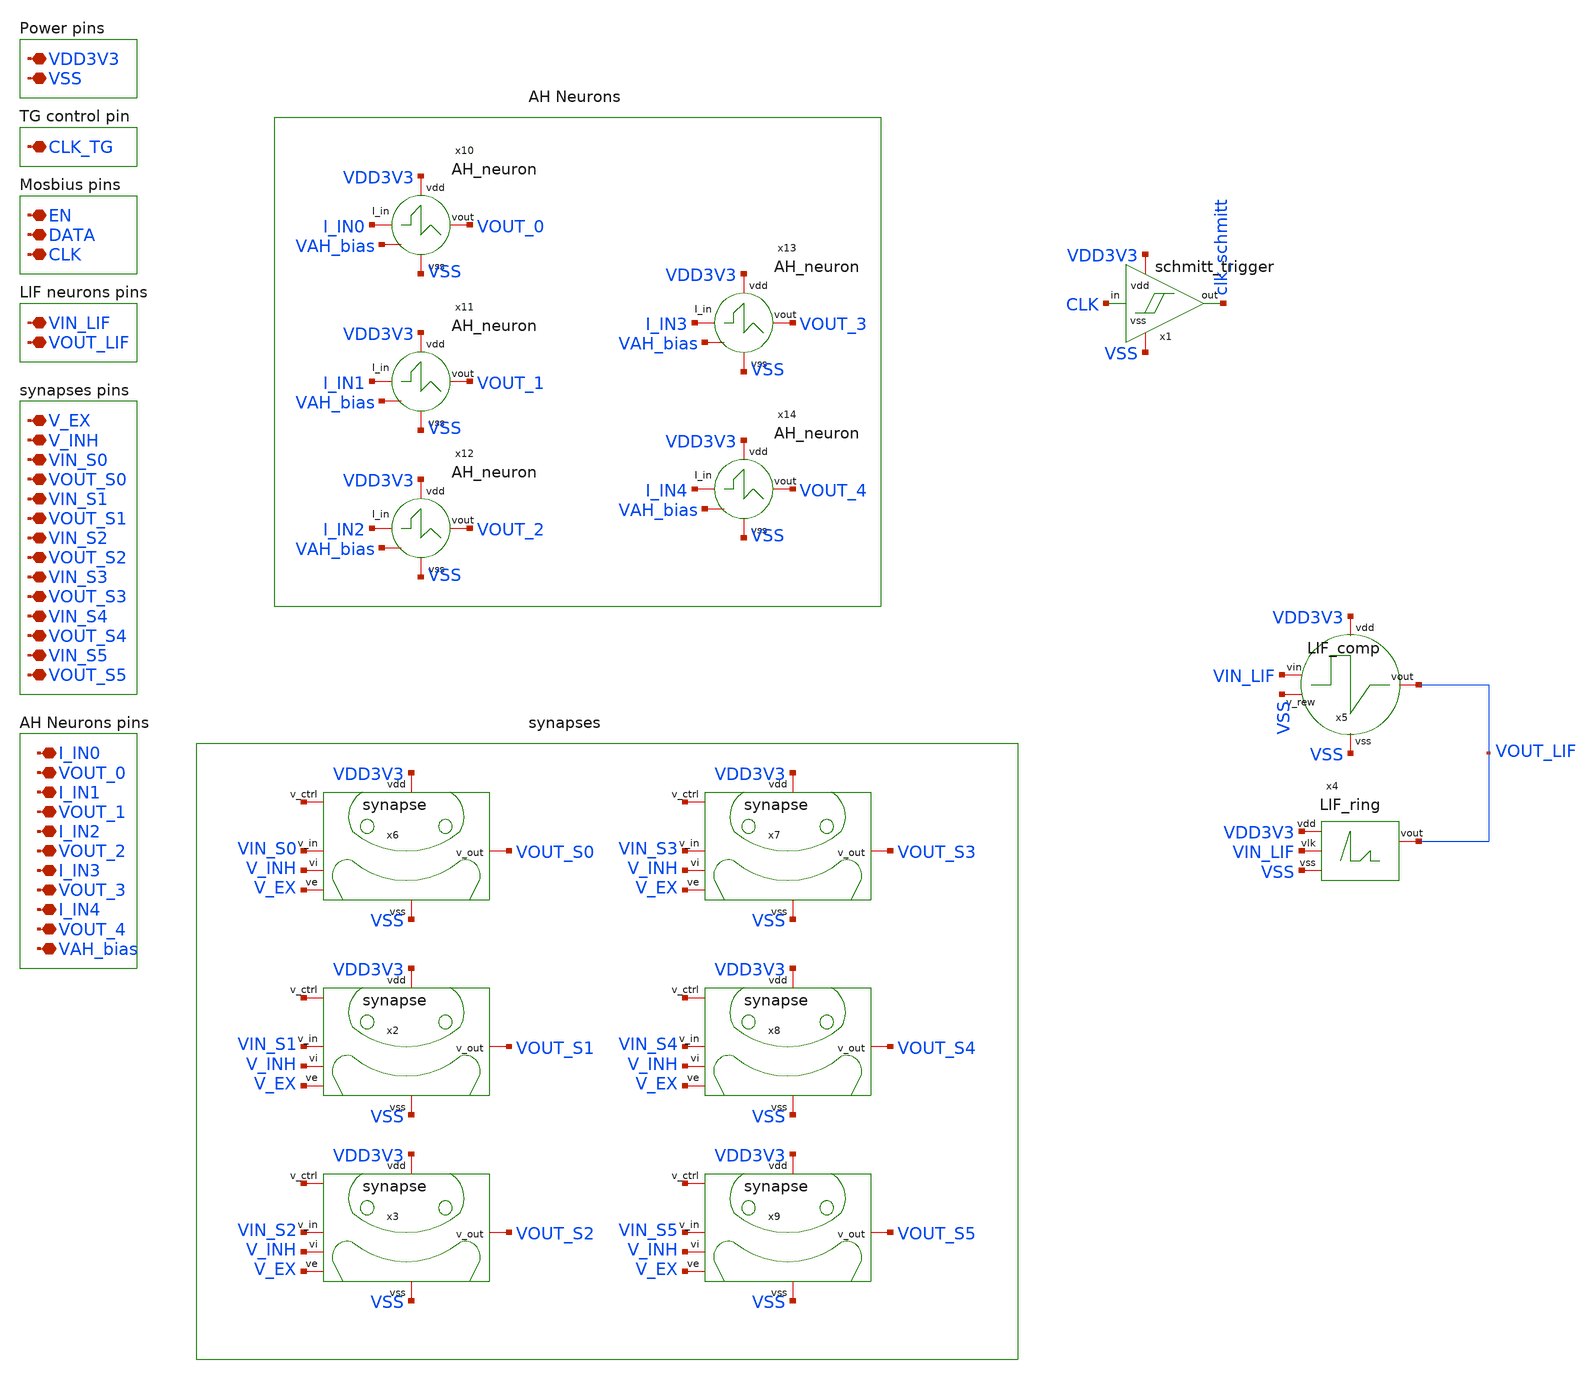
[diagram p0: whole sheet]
** sch_path: designs/libs/core_top/top.sch
**.subckt top CLK_TG I_IN0 VOUT_0 I_IN1 VOUT_1 I_IN2 VOUT_2 I_IN3 VOUT_3 VDD3V3 VSS VIN_LIF VOUT_LIF
*+ V_EX V_INH VIN_S0 VOUT_S0 VIN_S1 VOUT_S1 VIN_S2 VOUT_S2 EN DATA CLK I_IN4 VOUT_4 VIN_S3 VOUT_S3 VIN_S4
*+ VOUT_S4 VIN_S5 VOUT_S5 VAH_bias
*.iopin CLK_TG
*.iopin I_IN0
*.iopin VOUT_0
*.iopin I_IN1
*.iopin VOUT_1
*.iopin I_IN2
*.iopin VOUT_2
*.iopin I_IN3
*.iopin VOUT_3
*.iopin VDD3V3
*.iopin VSS
*.iopin VIN_LIF
*.iopin VOUT_LIF
*.iopin V_EX
*.iopin V_INH
*.iopin VIN_S0
*.iopin VOUT_S0
*.iopin VIN_S1
*.iopin VOUT_S1
*.iopin VIN_S2
*.iopin VOUT_S2
*.iopin EN
*.iopin DATA
*.iopin CLK
*.iopin I_IN4
*.iopin VOUT_4
*.iopin VIN_S3
*.iopin VOUT_S3
*.iopin VIN_S4
*.iopin VOUT_S4
*.iopin VIN_S5
*.iopin VOUT_S5
*.iopin VAH_bias
x4 VDD3V3 VIN_LIF VOUT_LIF VSS LIF_ring
x5 VDD3V3 VSS VIN_LIF VSS VOUT_LIF LIF_comp
x6 VDD3V3 VIN_S0 V_EX net1 VOUT_S0 V_INH VSS synapse
x2 VDD3V3 VIN_S1 V_EX net2 VOUT_S1 V_INH VSS synapse
x3 VDD3V3 VIN_S2 V_EX net3 VOUT_S2 V_INH VSS synapse
x7 VDD3V3 VIN_S3 V_EX net4 VOUT_S3 V_INH VSS synapse
x8 VDD3V3 VIN_S4 V_EX net5 VOUT_S4 V_INH VSS synapse
x9 VDD3V3 VIN_S5 V_EX net6 VOUT_S5 V_INH VSS synapse
x10 VDD3V3 I_IN0 VOUT_0 VSS VAH_bias AH_neuron
x11 VDD3V3 I_IN1 VOUT_1 VSS VAH_bias AH_neuron
x12 VDD3V3 I_IN2 VOUT_2 VSS VAH_bias AH_neuron
x13 VDD3V3 I_IN3 VOUT_3 VSS VAH_bias AH_neuron
x14 VDD3V3 I_IN4 VOUT_4 VSS VAH_bias AH_neuron
x1 clk_schmitt CLK VDD3V3 VSS schmitt_trigger
**.ends
.end
